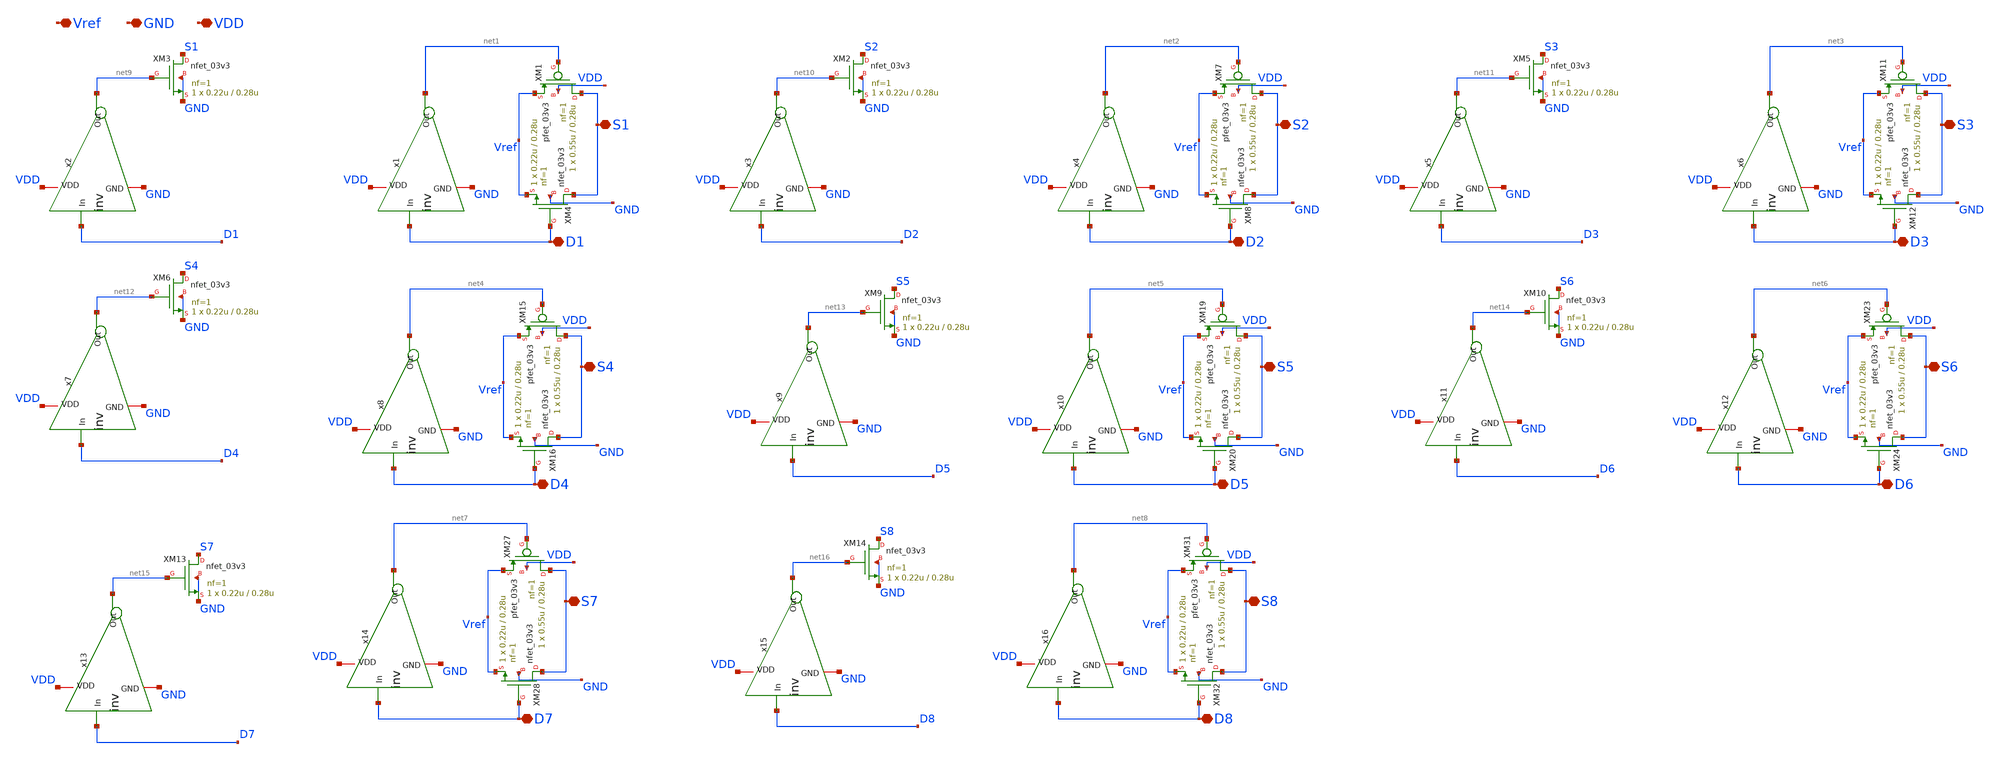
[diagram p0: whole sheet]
** sch_path: xschem/Switch_Array.sch
**.subckt Switch_Array VDD GND Vref S1 D1 S2 D2 S3 D3 S4 D4 S5 D5 S6 D6 S7 D7 S8 D8
*.iopin VDD
*.iopin GND
*.iopin Vref
*.iopin S1
*.iopin D1
*.iopin S2
*.iopin D2
*.iopin S3
*.iopin D3
*.iopin S4
*.iopin D4
*.iopin S5
*.iopin D5
*.iopin S6
*.iopin D6
*.iopin S7
*.iopin D7
*.iopin S8
*.iopin D8
XM3 S1 net9 GND GND nfet_03v3 L=0.28u W=0.22u nf=1 ad='int((nf+1)/2) * W/nf * 0.18u' as='int((nf+2)/2) * W/nf * 0.18u'
+ pd='2*int((nf+1)/2) * (W/nf + 0.18u)' ps='2*int((nf+2)/2) * (W/nf + 0.18u)' nrd='0.18u / W' nrs='0.18u / W'
+ sa=0 sb=0 sd=0 m=1
x2 VDD D1 net9 GND inv
XM1 S1 net1 Vref VDD pfet_03v3 L=0.28u W=0.55u nf=1 ad='int((nf+1)/2) * W/nf * 0.18u' as='int((nf+2)/2) * W/nf * 0.18u'
+ pd='2*int((nf+1)/2) * (W/nf + 0.18u)' ps='2*int((nf+2)/2) * (W/nf + 0.18u)' nrd='0.18u / W' nrs='0.18u / W'
+ sa=0 sb=0 sd=0 m=1
XM4 S1 D1 Vref GND nfet_03v3 L=0.28u W=0.22u nf=1 ad='int((nf+1)/2) * W/nf * 0.18u' as='int((nf+2)/2) * W/nf * 0.18u'
+ pd='2*int((nf+1)/2) * (W/nf + 0.18u)' ps='2*int((nf+2)/2) * (W/nf + 0.18u)' nrd='0.18u / W' nrs='0.18u / W'
+ sa=0 sb=0 sd=0 m=1
x1 VDD D1 net1 GND inv
x3 VDD D2 net10 GND inv
XM7 S2 net2 Vref VDD pfet_03v3 L=0.28u W=0.55u nf=1 ad='int((nf+1)/2) * W/nf * 0.18u' as='int((nf+2)/2) * W/nf * 0.18u'
+ pd='2*int((nf+1)/2) * (W/nf + 0.18u)' ps='2*int((nf+2)/2) * (W/nf + 0.18u)' nrd='0.18u / W' nrs='0.18u / W'
+ sa=0 sb=0 sd=0 m=1
XM8 S2 D2 Vref GND nfet_03v3 L=0.28u W=0.22u nf=1 ad='int((nf+1)/2) * W/nf * 0.18u' as='int((nf+2)/2) * W/nf * 0.18u'
+ pd='2*int((nf+1)/2) * (W/nf + 0.18u)' ps='2*int((nf+2)/2) * (W/nf + 0.18u)' nrd='0.18u / W' nrs='0.18u / W'
+ sa=0 sb=0 sd=0 m=1
x4 VDD D2 net2 GND inv
XM11 S3 net3 Vref VDD pfet_03v3 L=0.28u W=0.55u nf=1 ad='int((nf+1)/2) * W/nf * 0.18u' as='int((nf+2)/2) * W/nf * 0.18u'
+ pd='2*int((nf+1)/2) * (W/nf + 0.18u)' ps='2*int((nf+2)/2) * (W/nf + 0.18u)' nrd='0.18u / W' nrs='0.18u / W'
+ sa=0 sb=0 sd=0 m=1
XM12 S3 D3 Vref GND nfet_03v3 L=0.28u W=0.22u nf=1 ad='int((nf+1)/2) * W/nf * 0.18u' as='int((nf+2)/2) * W/nf * 0.18u'
+ pd='2*int((nf+1)/2) * (W/nf + 0.18u)' ps='2*int((nf+2)/2) * (W/nf + 0.18u)' nrd='0.18u / W' nrs='0.18u / W'
+ sa=0 sb=0 sd=0 m=1
x6 VDD D3 net3 GND inv
XM15 S4 net4 Vref VDD pfet_03v3 L=0.28u W=0.55u nf=1 ad='int((nf+1)/2) * W/nf * 0.18u' as='int((nf+2)/2) * W/nf * 0.18u'
+ pd='2*int((nf+1)/2) * (W/nf + 0.18u)' ps='2*int((nf+2)/2) * (W/nf + 0.18u)' nrd='0.18u / W' nrs='0.18u / W'
+ sa=0 sb=0 sd=0 m=1
XM16 S4 D4 Vref GND nfet_03v3 L=0.28u W=0.22u nf=1 ad='int((nf+1)/2) * W/nf * 0.18u' as='int((nf+2)/2) * W/nf * 0.18u'
+ pd='2*int((nf+1)/2) * (W/nf + 0.18u)' ps='2*int((nf+2)/2) * (W/nf + 0.18u)' nrd='0.18u / W' nrs='0.18u / W'
+ sa=0 sb=0 sd=0 m=1
x8 VDD D4 net4 GND inv
XM19 S5 net5 Vref VDD pfet_03v3 L=0.28u W=0.55u nf=1 ad='int((nf+1)/2) * W/nf * 0.18u' as='int((nf+2)/2) * W/nf * 0.18u'
+ pd='2*int((nf+1)/2) * (W/nf + 0.18u)' ps='2*int((nf+2)/2) * (W/nf + 0.18u)' nrd='0.18u / W' nrs='0.18u / W'
+ sa=0 sb=0 sd=0 m=1
XM20 S5 D5 Vref GND nfet_03v3 L=0.28u W=0.22u nf=1 ad='int((nf+1)/2) * W/nf * 0.18u' as='int((nf+2)/2) * W/nf * 0.18u'
+ pd='2*int((nf+1)/2) * (W/nf + 0.18u)' ps='2*int((nf+2)/2) * (W/nf + 0.18u)' nrd='0.18u / W' nrs='0.18u / W'
+ sa=0 sb=0 sd=0 m=1
x10 VDD D5 net5 GND inv
XM23 S6 net6 Vref VDD pfet_03v3 L=0.28u W=0.55u nf=1 ad='int((nf+1)/2) * W/nf * 0.18u' as='int((nf+2)/2) * W/nf * 0.18u'
+ pd='2*int((nf+1)/2) * (W/nf + 0.18u)' ps='2*int((nf+2)/2) * (W/nf + 0.18u)' nrd='0.18u / W' nrs='0.18u / W'
+ sa=0 sb=0 sd=0 m=1
XM24 S6 D6 Vref GND nfet_03v3 L=0.28u W=0.22u nf=1 ad='int((nf+1)/2) * W/nf * 0.18u' as='int((nf+2)/2) * W/nf * 0.18u'
+ pd='2*int((nf+1)/2) * (W/nf + 0.18u)' ps='2*int((nf+2)/2) * (W/nf + 0.18u)' nrd='0.18u / W' nrs='0.18u / W'
+ sa=0 sb=0 sd=0 m=1
x12 VDD D6 net6 GND inv
XM27 S7 net7 Vref VDD pfet_03v3 L=0.28u W=0.55u nf=1 ad='int((nf+1)/2) * W/nf * 0.18u' as='int((nf+2)/2) * W/nf * 0.18u'
+ pd='2*int((nf+1)/2) * (W/nf + 0.18u)' ps='2*int((nf+2)/2) * (W/nf + 0.18u)' nrd='0.18u / W' nrs='0.18u / W'
+ sa=0 sb=0 sd=0 m=1
XM28 S7 D7 Vref GND nfet_03v3 L=0.28u W=0.22u nf=1 ad='int((nf+1)/2) * W/nf * 0.18u' as='int((nf+2)/2) * W/nf * 0.18u'
+ pd='2*int((nf+1)/2) * (W/nf + 0.18u)' ps='2*int((nf+2)/2) * (W/nf + 0.18u)' nrd='0.18u / W' nrs='0.18u / W'
+ sa=0 sb=0 sd=0 m=1
x14 VDD D7 net7 GND inv
XM31 S8 net8 Vref VDD pfet_03v3 L=0.28u W=0.55u nf=1 ad='int((nf+1)/2) * W/nf * 0.18u' as='int((nf+2)/2) * W/nf * 0.18u'
+ pd='2*int((nf+1)/2) * (W/nf + 0.18u)' ps='2*int((nf+2)/2) * (W/nf + 0.18u)' nrd='0.18u / W' nrs='0.18u / W'
+ sa=0 sb=0 sd=0 m=1
XM32 S8 D8 Vref GND nfet_03v3 L=0.28u W=0.22u nf=1 ad='int((nf+1)/2) * W/nf * 0.18u' as='int((nf+2)/2) * W/nf * 0.18u'
+ pd='2*int((nf+1)/2) * (W/nf + 0.18u)' ps='2*int((nf+2)/2) * (W/nf + 0.18u)' nrd='0.18u / W' nrs='0.18u / W'
+ sa=0 sb=0 sd=0 m=1
x16 VDD D8 net8 GND inv
XM2 S2 net10 GND GND nfet_03v3 L=0.28u W=0.22u nf=1 ad='int((nf+1)/2) * W/nf * 0.18u' as='int((nf+2)/2) * W/nf * 0.18u'
+ pd='2*int((nf+1)/2) * (W/nf + 0.18u)' ps='2*int((nf+2)/2) * (W/nf + 0.18u)' nrd='0.18u / W' nrs='0.18u / W'
+ sa=0 sb=0 sd=0 m=1
x5 VDD D3 net11 GND inv
XM5 S3 net11 GND GND nfet_03v3 L=0.28u W=0.22u nf=1 ad='int((nf+1)/2) * W/nf * 0.18u' as='int((nf+2)/2) * W/nf * 0.18u'
+ pd='2*int((nf+1)/2) * (W/nf + 0.18u)' ps='2*int((nf+2)/2) * (W/nf + 0.18u)' nrd='0.18u / W' nrs='0.18u / W'
+ sa=0 sb=0 sd=0 m=1
XM6 S4 net12 GND GND nfet_03v3 L=0.28u W=0.22u nf=1 ad='int((nf+1)/2) * W/nf * 0.18u' as='int((nf+2)/2) * W/nf * 0.18u'
+ pd='2*int((nf+1)/2) * (W/nf + 0.18u)' ps='2*int((nf+2)/2) * (W/nf + 0.18u)' nrd='0.18u / W' nrs='0.18u / W'
+ sa=0 sb=0 sd=0 m=1
x7 VDD D4 net12 GND inv
XM9 S5 net13 GND GND nfet_03v3 L=0.28u W=0.22u nf=1 ad='int((nf+1)/2) * W/nf * 0.18u' as='int((nf+2)/2) * W/nf * 0.18u'
+ pd='2*int((nf+1)/2) * (W/nf + 0.18u)' ps='2*int((nf+2)/2) * (W/nf + 0.18u)' nrd='0.18u / W' nrs='0.18u / W'
+ sa=0 sb=0 sd=0 m=1
x9 VDD D5 net13 GND inv
XM10 S6 net14 GND GND nfet_03v3 L=0.28u W=0.22u nf=1 ad='int((nf+1)/2) * W/nf * 0.18u' as='int((nf+2)/2) * W/nf * 0.18u'
+ pd='2*int((nf+1)/2) * (W/nf + 0.18u)' ps='2*int((nf+2)/2) * (W/nf + 0.18u)' nrd='0.18u / W' nrs='0.18u / W'
+ sa=0 sb=0 sd=0 m=1
x11 VDD D6 net14 GND inv
XM13 S7 net15 GND GND nfet_03v3 L=0.28u W=0.22u nf=1 ad='int((nf+1)/2) * W/nf * 0.18u' as='int((nf+2)/2) * W/nf * 0.18u'
+ pd='2*int((nf+1)/2) * (W/nf + 0.18u)' ps='2*int((nf+2)/2) * (W/nf + 0.18u)' nrd='0.18u / W' nrs='0.18u / W'
+ sa=0 sb=0 sd=0 m=1
x13 VDD D7 net15 GND inv
XM14 S8 net16 GND GND nfet_03v3 L=0.28u W=0.22u nf=1 ad='int((nf+1)/2) * W/nf * 0.18u' as='int((nf+2)/2) * W/nf * 0.18u'
+ pd='2*int((nf+1)/2) * (W/nf + 0.18u)' ps='2*int((nf+2)/2) * (W/nf + 0.18u)' nrd='0.18u / W' nrs='0.18u / W'
+ sa=0 sb=0 sd=0 m=1
x15 VDD D8 net16 GND inv
**.ends

* expanding   symbol:  inv.sym # of pins=4
** sym_path: xschem/inv.sym
** sch_path: xschem/inv.sch
.subckt inv VDD In Out GND
*.iopin VDD
*.iopin GND
*.ipin In
*.opin Out
XM3 Out In GND GND nfet_03v3 L=0.28u W=0.22u nf=1 ad='int((nf+1)/2) * W/nf * 0.18u' as='int((nf+2)/2) * W/nf * 0.18u'
+ pd='2*int((nf+1)/2) * (W/nf + 0.18u)' ps='2*int((nf+2)/2) * (W/nf + 0.18u)' nrd='0.18u / W' nrs='0.18u / W'
+ sa=0 sb=0 sd=0 m=1
XM2 Out In VDD VDD pfet_03v3 L=0.28u W=0.55u nf=1 ad='int((nf+1)/2) * W/nf * 0.18u' as='int((nf+2)/2) * W/nf * 0.18u'
+ pd='2*int((nf+1)/2) * (W/nf + 0.18u)' ps='2*int((nf+2)/2) * (W/nf + 0.18u)' nrd='0.18u / W' nrs='0.18u / W'
+ sa=0 sb=0 sd=0 m=1
.ends

.end
